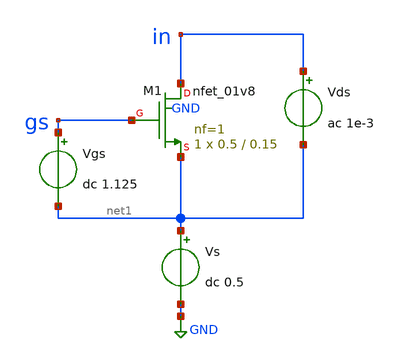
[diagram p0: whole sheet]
** sch_path: Amplifier_Inv/xschem/v2/tb_res.sch
**.subckt tb_res
Vgs gs net1 dc 1.125
Vds in net1 ac 1e-3
XM1 in gs net1 GND sky130_fd_pr__nfet_01v8 L=0.15 W=0.5 nf=1 ad='int((nf+1)/2) * W/nf * 0.29' as='int((nf+2)/2) * W/nf * 0.29'
+ pd='2*int((nf+1)/2) * (W/nf + 0.29)' ps='2*int((nf+2)/2) * (W/nf + 0.29)' nrd='0.29 / W' nrs='0.29 / W'
+ sa=0 sb=0 sd=0 mult=1 m=1
Vs net1 GND dc 0.5
**** begin user architecture code

** opencircuitdesign pdks install
.lib $::SKYWATER_MODELS/sky130.lib.spice tt



.control

  let start_vgs = 0.2
  let stop_vgs = 0.8
  let delta_vgs = 0.05
  let vgs_act = start_vgs

  while vgs_act le stop_vgs
  alter vgs dc vgs_act
  ac dec 100 0.1 100k
  let r = v(in)/(-i(Vds))
  save all
  write tb_inv_sky130_a_res_AC_v2.raw r
  set appendwrite
  let vgs_act = vgs_act + delta_vgs
  end

.endc


**** end user architecture code
**.ends
.GLOBAL GND
.end
